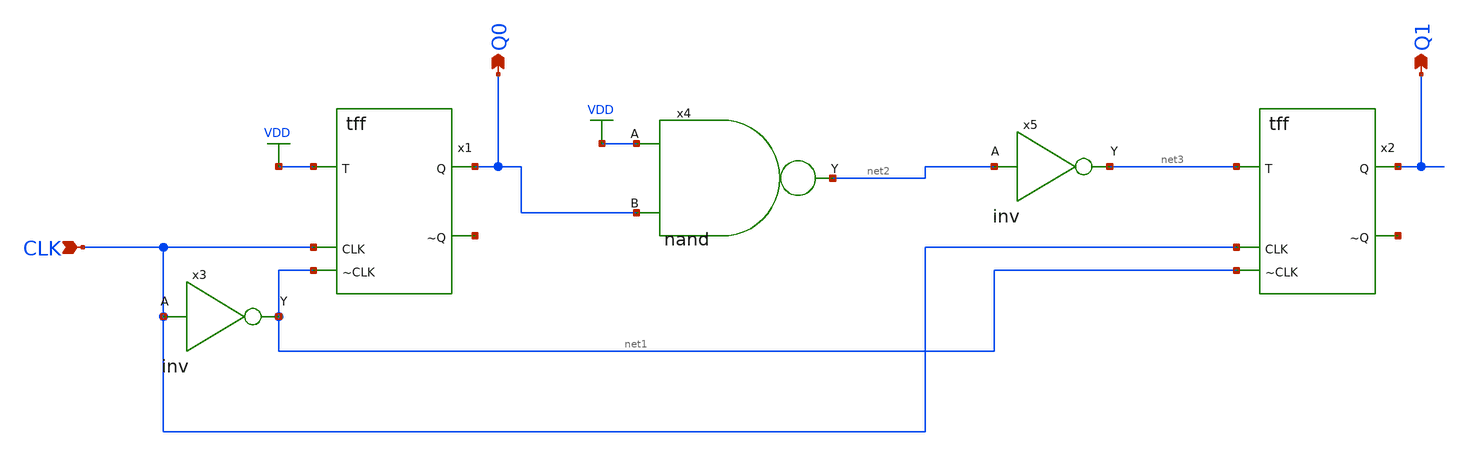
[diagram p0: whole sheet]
** sch_path: circuits/xschem/counter_2.sch
**.subckt counter_2 CLK Q0 Q1
*.ipin CLK
*.opin Q0
*.opin Q1
x1 VDD Q0 CLK net1 net4 tff
x2 net3 Q1 CLK net1 net5 tff
x3 net1 CLK inv
x4 VDD net2 Q0 nand
x5 net3 net2 inv
**.ends
.GLOBAL VDD
.end
